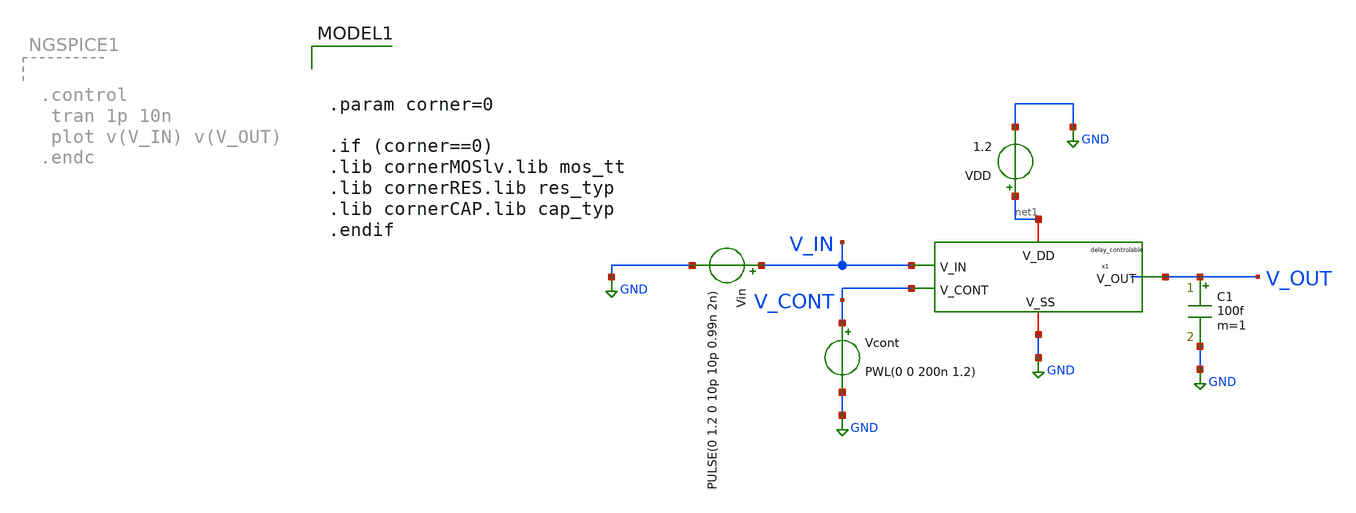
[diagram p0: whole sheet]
** sch_path: others/probe_1.sch
**.subckt probe_1
VDD net1 GND 1.2
Vin V_IN GND PULSE(0 1.2 0 10p 10p 0.99n 2n)
C1 V_OUT GND 100f m=1
Vcont V_CONT GND PWL(0 0 200n 1.2)
x1 net1 V_OUT V_IN V_CONT GND delay_controlable
**** begin user architecture code


.param corner=0

.if (corner==0)
.lib cornerMOSlv.lib mos_tt
.lib cornerRES.lib res_typ
.lib cornerCAP.lib cap_typ
.endif



.control
* ---- settings you tweak ----
   * ---- user settings ----
  let vlow  = 0
  let vhigh = 1.2
  let v50   = vlow + 0.5*(vhigh - vlow)

  let start_edge = 0     ; skip early edges (settling)
  let N = 200             ; number of phase samples

  tran 1p 200n

  * ---- allocate vectors ----
  let tvec   = vector(N)
  let phivec = vector(N)

  let k = 0
  let i = start_edge

  while k < N
    * crossing times
    meas tran tin      WHEN v(V_IN)=v50  RISE=i
    meas tran tout     WHEN v(V_OUT)=v50 RISE=i
    meas tran tin_next WHEN v(V_IN)=v50  RISE=(i+1)

    * delay + period
    let dt = tout - tin
    let T  = tin_next - tin

    * phase in degrees (per-cycle)
    let phi = 360*dt/T
    let phi = phi - 360*floor(phi/360)

    * store sample at time = tin
    let tvec[k]   = tin
    let phivec[k] = phi

    let k = k + 1
    let i = i + 1
  end

  * plot phase vs time (one point per cycle)
  plot phivec vs tvec
  plot v(V_IN) v(V_OUT) v(V_CONT)
  plot phivec vs v(V_CONT)
.endc


**** end user architecture code
**.ends

* expanding   symbol:  /foss/designs/DLL/2026/clemen/delay_controlable.sym # of pins=5
** sym_path: others/clemen/delay_controlable.sym
** sch_path: others/clemen/delay_controlable.sch
.subckt delay_controlable V_DD V_OUT V_IN V_CONT V_SS
*.iopin V_DD
*.iopin V_SS
*.ipin V_IN
*.ipin V_CONT
*.opin V_OUT
XM1 V_OUT V_IN net3 V_SS sg13_lv_nmos w=2u l=0.13u ng=1 m=1 mm_ok=1
XM2 net3 V_CONT V_SS V_SS sg13_lv_nmos w=5u l=0.16u ng=1 m=1 mm_ok=1
XM3 net1 V_CONT V_SS V_SS sg13_lv_nmos w=2u l=0.25u ng=1 m=1 mm_ok=1
XM4 V_OUT V_IN net2 V_DD sg13_lv_pmos w=5u l=0.13u ng=1 m=1 mm_ok=1
XM5 net2 net1 V_DD V_DD sg13_lv_pmos w=5u l=0.16u ng=1 m=1 mm_ok=1
XM6 net1 net1 V_DD V_DD sg13_lv_pmos w=2.24u l=0.13u ng=1 m=1 mm_ok=1
.ends

.GLOBAL GND
.end
